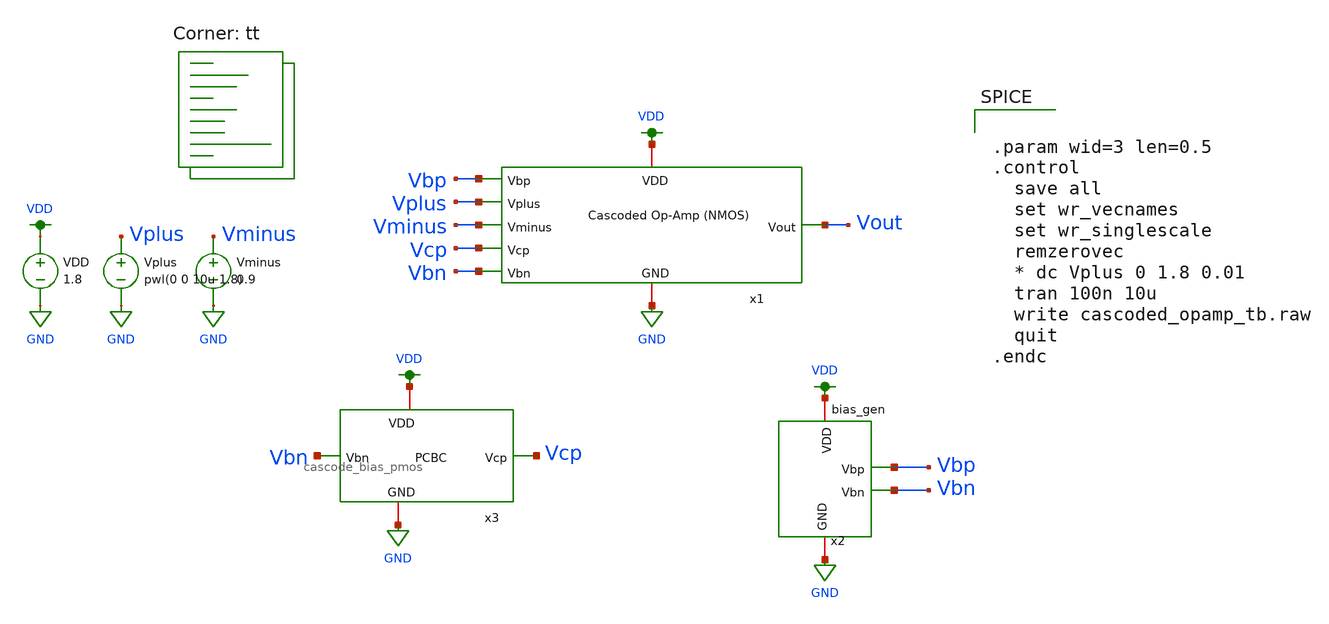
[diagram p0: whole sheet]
** sch_path: final/schematics/cascoded_opamp_tb.sch
**.subckt cascoded_opamp_tb
x1 Vbp Vplus Vminus Vcp Vbn VDD GND Vout cascoded_opamp
x2 VDD Vbp Vbn GND bias_gen
VDD VDD GND 1.8
x3 Vbn VDD GND Vcp cascode_bias_pmos
Vplus Vplus GND pwl(0 0 10u 1.8)
Vminus Vminus GND 0.9
**** begin user architecture code
.lib $::SKYWATER_MODELS/sky130.lib.spice tt


.param wid=3 len=0.5
.control
  save all
  set wr_vecnames
  set wr_singlescale
  remzerovec
  * dc Vplus 0 1.8 0.01
  tran 100n 10u
  write cascoded_opamp_tb.raw
  quit
.endc


**** end user architecture code
**.ends

* expanding   symbol:  cascoded_opamp.sym # of pins=8
** sym_path: final/schematics/cascoded_opamp.sym
** sch_path: final/schematics/cascoded_opamp.sch
.subckt cascoded_opamp Vbp Vplus Vminus Vcp Vbn VDD GND Vout
*.ipin Vbp
*.ipin Vplus
*.ipin Vminus
*.ipin Vcp
*.ipin Vbn
*.iopin VDD
*.iopin GND
*.opin Vout
XM1 net1 Vbn GND GND sky130_fd_pr__nfet_01v8 L={len} W={wid} nf=1 ad='int((nf+1)/2) * W/nf * 0.29' as='int((nf+2)/2) * W/nf * 0.29'
+ pd='2*int((nf+1)/2) * (W/nf + 0.29)' ps='2*int((nf+2)/2) * (W/nf + 0.29)' nrd='0.29 / W' nrs='0.29 / W'
+ sa=0 sb=0 sd=0 mult=1 m=1
XM2 net2 Vplus net1 GND sky130_fd_pr__nfet_01v8 L={len} W={wid} nf=1 ad='int((nf+1)/2) * W/nf * 0.29'
+ as='int((nf+2)/2) * W/nf * 0.29' pd='2*int((nf+1)/2) * (W/nf + 0.29)' ps='2*int((nf+2)/2) * (W/nf + 0.29)'
+ nrd='0.29 / W' nrs='0.29 / W' sa=0 sb=0 sd=0 mult=1 m=1
XM3 net1 Vminus net3 GND sky130_fd_pr__nfet_01v8 L={len} W={wid} nf=1 ad='int((nf+1)/2) * W/nf * 0.29'
+ as='int((nf+2)/2) * W/nf * 0.29' pd='2*int((nf+1)/2) * (W/nf + 0.29)' ps='2*int((nf+2)/2) * (W/nf + 0.29)'
+ nrd='0.29 / W' nrs='0.29 / W' sa=0 sb=0 sd=0 mult=1 m=1
XM4 net2 Vbp VDD VDD sky130_fd_pr__pfet_01v8 L={len} W={wid} nf=1 ad='int((nf+1)/2) * W/nf * 0.29' as='int((nf+2)/2) * W/nf * 0.29'
+ pd='2*int((nf+1)/2) * (W/nf + 0.29)' ps='2*int((nf+2)/2) * (W/nf + 0.29)' nrd='0.29 / W' nrs='0.29 / W'
+ sa=0 sb=0 sd=0 mult=1 m=1
XM5 net3 Vbp VDD VDD sky130_fd_pr__pfet_01v8 L={len} W={wid} nf=1 ad='int((nf+1)/2) * W/nf * 0.29' as='int((nf+2)/2) * W/nf * 0.29'
+ pd='2*int((nf+1)/2) * (W/nf + 0.29)' ps='2*int((nf+2)/2) * (W/nf + 0.29)' nrd='0.29 / W' nrs='0.29 / W'
+ sa=0 sb=0 sd=0 mult=1 m=1
XM6 net4 Vcp net2 VDD sky130_fd_pr__pfet_01v8 L={len} W={wid} nf=1 ad='int((nf+1)/2) * W/nf * 0.29' as='int((nf+2)/2) * W/nf * 0.29'
+ pd='2*int((nf+1)/2) * (W/nf + 0.29)' ps='2*int((nf+2)/2) * (W/nf + 0.29)' nrd='0.29 / W' nrs='0.29 / W'
+ sa=0 sb=0 sd=0 mult=1 m=1
XM7 Vout Vcp net3 VDD sky130_fd_pr__pfet_01v8 L={len} W={wid} nf=1 ad='int((nf+1)/2) * W/nf * 0.29' as='int((nf+2)/2) * W/nf * 0.29'
+ pd='2*int((nf+1)/2) * (W/nf + 0.29)' ps='2*int((nf+2)/2) * (W/nf + 0.29)' nrd='0.29 / W' nrs='0.29 / W'
+ sa=0 sb=0 sd=0 mult=1 m=1
XM8 GND net4 net4 GND sky130_fd_pr__nfet_01v8 L={len} W={wid} nf=1 ad='int((nf+1)/2) * W/nf * 0.29' as='int((nf+2)/2) * W/nf * 0.29'
+ pd='2*int((nf+1)/2) * (W/nf + 0.29)' ps='2*int((nf+2)/2) * (W/nf + 0.29)' nrd='0.29 / W' nrs='0.29 / W'
+ sa=0 sb=0 sd=0 mult=1 m=1
XM9 Vout net4 GND GND sky130_fd_pr__nfet_01v8 L={len} W={wid} nf=1 ad='int((nf+1)/2) * W/nf * 0.29' as='int((nf+2)/2) * W/nf * 0.29'
+ pd='2*int((nf+1)/2) * (W/nf + 0.29)' ps='2*int((nf+2)/2) * (W/nf + 0.29)' nrd='0.29 / W' nrs='0.29 / W'
+ sa=0 sb=0 sd=0 mult=1 m=1
**** begin user architecture code


.param wid=3 len=0.5


**** end user architecture code
.ends


* expanding   symbol:  /home/madvlsi/Documents/madvlsi/final/schematics/bias_gen/bias_gen.sym # of
*+ pins=4
** sym_path: final/schematics/bias_gen/bias_gen.sym
** sch_path: final/schematics/bias_gen/bias_gen.sch
.subckt bias_gen VDD Vbp Vbn GND
*.iopin VDD
*.opin Vbp
*.iopin GND
*.opin Vbn
**** begin user architecture code

.param len=0.5 wid=3

**** end user architecture code
XM10 net3 net1 net1 GND sky130_fd_pr__nfet_01v8 L={len} W={wid} nf=1 ad='int((nf+1)/2) * W/nf * 0.29'
+ as='int((nf+2)/2) * W/nf * 0.29' pd='2*int((nf+1)/2) * (W/nf + 0.29)' ps='2*int((nf+2)/2) * (W/nf + 0.29)'
+ nrd='0.29 / W' nrs='0.29 / W' sa=0 sb=0 sd=0 mult=10 m=10
XM11 Vbn Vbn GND GND sky130_fd_pr__nfet_01v8 L={len} W={wid} nf=1 ad='int((nf+1)/2) * W/nf * 0.29' as='int((nf+2)/2) * W/nf * 0.29'
+ pd='2*int((nf+1)/2) * (W/nf + 0.29)' ps='2*int((nf+2)/2) * (W/nf + 0.29)' nrd='0.29 / W' nrs='0.29 / W'
+ sa=0 sb=0 sd=0 mult=1 m=1
XM12 GND Vbp GND GND sky130_fd_pr__nfet_01v8 L=10 W=10 nf=1 ad='int((nf+1)/2) * W/nf * 0.29' as='int((nf+2)/2) * W/nf * 0.29'
+ pd='2*int((nf+1)/2) * (W/nf + 0.29)' ps='2*int((nf+2)/2) * (W/nf + 0.29)' nrd='0.29 / W' nrs='0.29 / W'
+ sa=0 sb=0 sd=0 mult=1 m=1
XM13 VDD Vbp net1 VDD sky130_fd_pr__pfet_01v8 L={len} W={wid} nf=1 ad='int((nf+1)/2) * W/nf * 0.29' as='int((nf+2)/2) * W/nf * 0.29'
+ pd='2*int((nf+1)/2) * (W/nf + 0.29)' ps='2*int((nf+2)/2) * (W/nf + 0.29)' nrd='0.29 / W' nrs='0.29 / W'
+ sa=0 sb=0 sd=0 mult=1 m=1
XM14 GND Vbn Vbp GND sky130_fd_pr__nfet_01v8 L={len} W={wid} nf=1 ad='int((nf+1)/2) * W/nf * 0.29' as='int((nf+2)/2) * W/nf * 0.29'
+ pd='2*int((nf+1)/2) * (W/nf + 0.29)' ps='2*int((nf+2)/2) * (W/nf + 0.29)' nrd='0.29 / W' nrs='0.29 / W'
+ sa=0 sb=0 sd=0 mult=1 m=1
XM15 net2 net1 GND GND sky130_fd_pr__nfet_01v8 L={len} W={wid} nf=1 ad='int((nf+1)/2) * W/nf * 0.29'
+ as='int((nf+2)/2) * W/nf * 0.29' pd='2*int((nf+1)/2) * (W/nf + 0.29)' ps='2*int((nf+2)/2) * (W/nf + 0.29)'
+ nrd='0.29 / W' nrs='0.29 / W' sa=0 sb=0 sd=0 mult=1 m=1
XM16 VDD net2 net2 VDD sky130_fd_pr__pfet_01v8 L={len} W={wid} nf=1 ad='int((nf+1)/2) * W/nf * 0.29'
+ as='int((nf+2)/2) * W/nf * 0.29' pd='2*int((nf+1)/2) * (W/nf + 0.29)' ps='2*int((nf+2)/2) * (W/nf + 0.29)'
+ nrd='0.29 / W' nrs='0.29 / W' sa=0 sb=0 sd=0 mult=1 m=1
XM17 Vbp net2 VDD VDD sky130_fd_pr__pfet_01v8 L={len} W={wid} nf=1 ad='int((nf+1)/2) * W/nf * 0.29' as='int((nf+2)/2) * W/nf * 0.29'
+ pd='2*int((nf+1)/2) * (W/nf + 0.29)' ps='2*int((nf+2)/2) * (W/nf + 0.29)' nrd='0.29 / W' nrs='0.29 / W'
+ sa=0 sb=0 sd=0 mult=1 m=1
XM18 Vbn Vbp VDD VDD sky130_fd_pr__pfet_01v8 L={len} W={wid} nf=1 ad='int((nf+1)/2) * W/nf * 0.29' as='int((nf+2)/2) * W/nf * 0.29'
+ pd='2*int((nf+1)/2) * (W/nf + 0.29)' ps='2*int((nf+2)/2) * (W/nf + 0.29)' nrd='0.29 / W' nrs='0.29 / W'
+ sa=0 sb=0 sd=0 mult=1 m=1
XR2 GND net3 GND sky130_fd_pr__res_high_po_0p35 L=9 mult=1 m=1
.ends


* expanding   symbol:  cascode_bias_pmos.sym # of pins=4
** sym_path: final/schematics/cascode_bias_pmos.sym
** sch_path: final/schematics/cascode_bias_pmos.sch
.subckt cascode_bias_pmos Vbn VDD GND Vcp
*.ipin Vbn
*.iopin VDD
*.iopin GND
*.opin Vcp
XM1 VDD net2 net1 VDD sky130_fd_pr__pfet_01v8 L={len} W={wid} nf=1 ad='int((nf+1)/2) * W/nf * 0.29' as='int((nf+2)/2) * W/nf * 0.29'
+ pd='2*int((nf+1)/2) * (W/nf + 0.29)' ps='2*int((nf+2)/2) * (W/nf + 0.29)' nrd='0.29 / W' nrs='0.29 / W'
+ sa=0 sb=0 sd=0 mult=1 m=1
XM2 net1 net2 net2 VDD sky130_fd_pr__pfet_01v8 L={len} W={wid} nf=1 ad='int((nf+1)/2) * W/nf * 0.29'
+ as='int((nf+2)/2) * W/nf * 0.29' pd='2*int((nf+1)/2) * (W/nf + 0.29)' ps='2*int((nf+2)/2) * (W/nf + 0.29)'
+ nrd='0.29 / W' nrs='0.29 / W' sa=0 sb=0 sd=0 mult=1 m=1
XM3 net1 net2 net2 VDD sky130_fd_pr__pfet_01v8 L={len} W={wid} nf=1 ad='int((nf+1)/2) * W/nf * 0.29'
+ as='int((nf+2)/2) * W/nf * 0.29' pd='2*int((nf+1)/2) * (W/nf + 0.29)' ps='2*int((nf+2)/2) * (W/nf + 0.29)'
+ nrd='0.29 / W' nrs='0.29 / W' sa=0 sb=0 sd=0 mult=1 m=1
XM4 net1 Vcp Vcp VDD sky130_fd_pr__pfet_01v8 L={len} W={wid} nf=1 ad='int((nf+1)/2) * W/nf * 0.29' as='int((nf+2)/2) * W/nf * 0.29'
+ pd='2*int((nf+1)/2) * (W/nf + 0.29)' ps='2*int((nf+2)/2) * (W/nf + 0.29)' nrd='0.29 / W' nrs='0.29 / W'
+ sa=0 sb=0 sd=0 mult=1 m=1
XM5 net3 Vbn net2 GND sky130_fd_pr__nfet_01v8 L={len} W={wid} nf=1 ad='int((nf+1)/2) * W/nf * 0.29' as='int((nf+2)/2) * W/nf * 0.29'
+ pd='2*int((nf+1)/2) * (W/nf + 0.29)' ps='2*int((nf+2)/2) * (W/nf + 0.29)' nrd='0.29 / W' nrs='0.29 / W'
+ sa=0 sb=0 sd=0 mult=1 m=1
XM6 net4 Vbn net3 GND sky130_fd_pr__nfet_01v8 L={len} W={wid} nf=1 ad='int((nf+1)/2) * W/nf * 0.29' as='int((nf+2)/2) * W/nf * 0.29'
+ pd='2*int((nf+1)/2) * (W/nf + 0.29)' ps='2*int((nf+2)/2) * (W/nf + 0.29)' nrd='0.29 / W' nrs='0.29 / W'
+ sa=0 sb=0 sd=0 mult=1 m=1
XM7 GND Vbn net4 GND sky130_fd_pr__nfet_01v8 L={len} W={wid} nf=1 ad='int((nf+1)/2) * W/nf * 0.29' as='int((nf+2)/2) * W/nf * 0.29'
+ pd='2*int((nf+1)/2) * (W/nf + 0.29)' ps='2*int((nf+2)/2) * (W/nf + 0.29)' nrd='0.29 / W' nrs='0.29 / W'
+ sa=0 sb=0 sd=0 mult=1 m=1
XM8 GND Vbn Vcp GND sky130_fd_pr__nfet_01v8 L={len} W={wid} nf=1 ad='int((nf+1)/2) * W/nf * 0.29' as='int((nf+2)/2) * W/nf * 0.29'
+ pd='2*int((nf+1)/2) * (W/nf + 0.29)' ps='2*int((nf+2)/2) * (W/nf + 0.29)' nrd='0.29 / W' nrs='0.29 / W'
+ sa=0 sb=0 sd=0 mult=1 m=1
**** begin user architecture code

.param len=0.5 wid=3

**** end user architecture code
.ends

.GLOBAL VDD
.GLOBAL GND
.end
